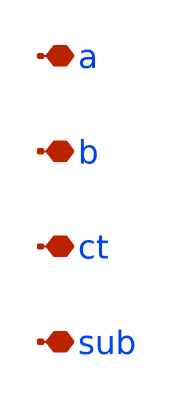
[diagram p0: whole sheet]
** sch_path: sch/inductor/inductor_placeholder_rlc.sch
**.subckt inductor_placeholder_rlc a b ct sub
*.iopin a
*.iopin b
*.iopin ct
*.iopin sub
**** begin user architecture code


R31 net27 b r=1e-2
R26 a net23 r=1e-2
C24 net35 net27 c=103.1e-15
C25 net23 net37 c=357e-15
C1 net27 net31 c=357e-15
R3 sub net31 r=3.67e3
R2 net41 net27 r=1.7645
R13 net23 net35 r=9.312
R10 sub net37 r=3.67e3
R9 net23 net39 r=1.7645
L1 net39 ct l=2.895e-9
L2 ct net41 l=2.895e-9


**** end user architecture code
**.ends
.end
